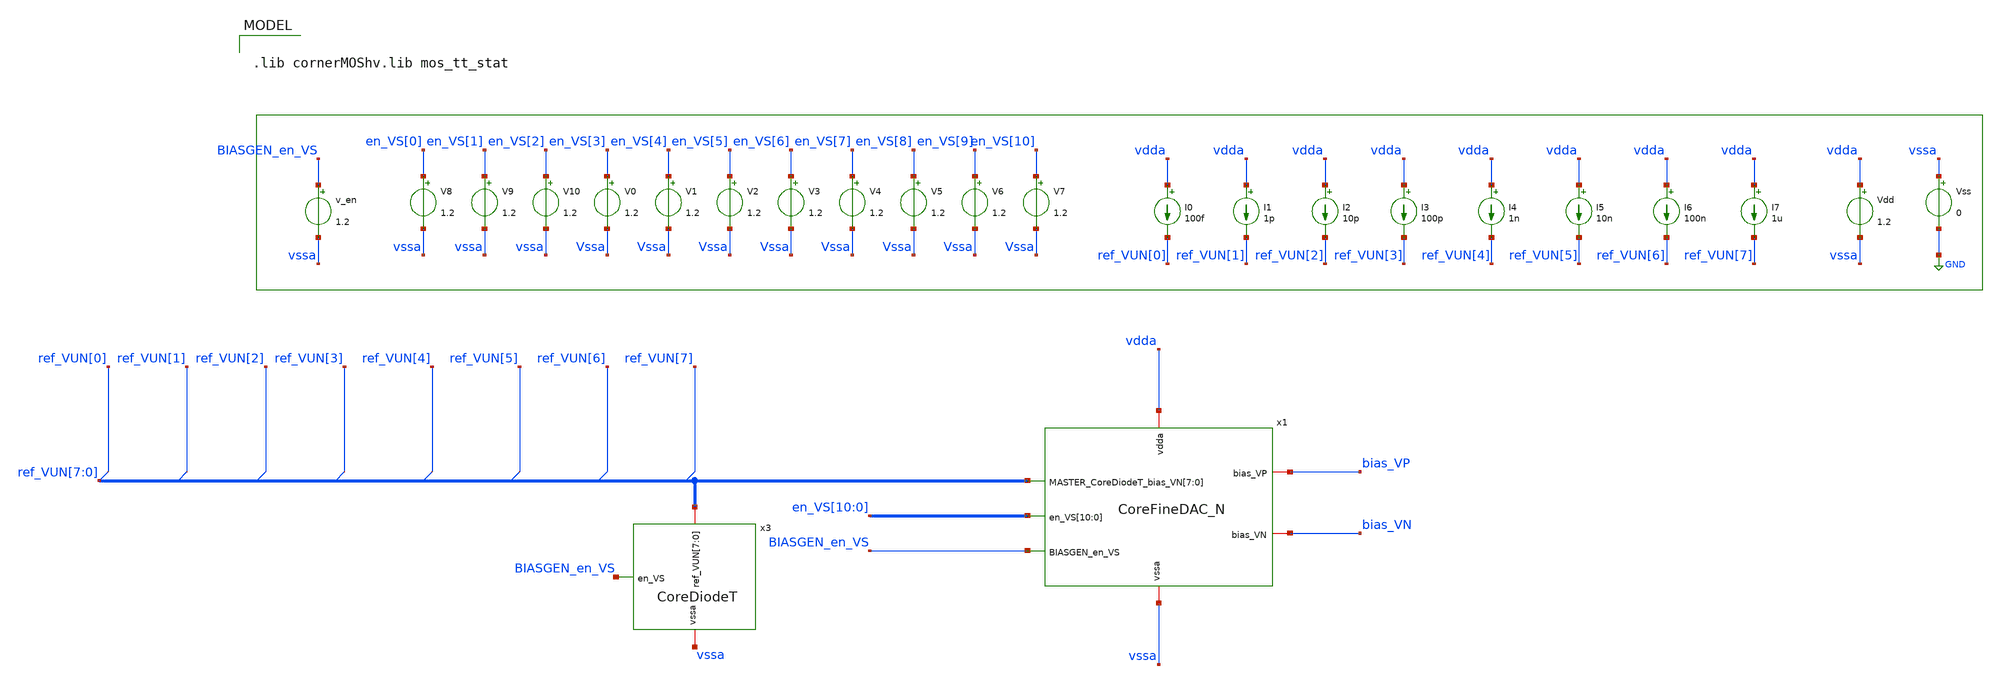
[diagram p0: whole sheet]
** sch_path: test_bench/CoreFineDAC_N_mc_dc_tb.sch
**.subckt CoreFineDAC_N_mc_dc_tb
Vdd vdda vssa 1.2
V0 en_VS[3] Vssa 1.2
Vss vssa GND 0
V1 en_VS[4] Vssa 1.2
V2 en_VS[5] Vssa 1.2
V3 en_VS[6] Vssa 1.2
V4 en_VS[7] Vssa 1.2
V5 en_VS[8] Vssa 1.2
V6 en_VS[9] Vssa 1.2
V7 en_VS[10] Vssa 1.2
V8 en_VS[0] vssa 1.2
V9 en_VS[1] vssa 1.2
V10 en_VS[2] vssa 1.2
I0 vdda ref_VUN[0] 100f
I1 vdda ref_VUN[1] 1p
I2 vdda ref_VUN[2] 10p
I3 vdda ref_VUN[3] 100p
I4 vdda ref_VUN[4] 1n
I6 vdda ref_VUN[6] 100n
I5 vdda ref_VUN[5] 10n
I7 vdda ref_VUN[7] 1u
v_en BIASGEN_en_VS vssa 1.2
x1 en_VS[10] en_VS[9] en_VS[8] en_VS[7] en_VS[6] en_VS[5] en_VS[4] en_VS[3] en_VS[2] en_VS[1]
+ en_VS[0] vssa vdda bias_VP bias_VN ref_VUN[7] ref_VUN[6] ref_VUN[5] ref_VUN[4] ref_VUN[3] ref_VUN[2]
+ ref_VUN[1] ref_VUN[0] BIASGEN_en_VS CoreFineDAC_N
x3 ref_VUN[7] ref_VUN[6] ref_VUN[5] ref_VUN[4] ref_VUN[3] ref_VUN[2] ref_VUN[1] ref_VUN[0] vssa
+ BIASGEN_en_VS CoreDiodeT
**** begin user architecture code

.lib cornerMOShv.lib mos_tt_stat



.param mm_ok=1
.param mc_ok=1
.param temp=27
.options abstol=1e-14
.options gmin=1e-14
.options gmindc=1e-14
.control


let mc_runs = 300
let run = 0
dowhile run < mc_runs

nodeset v(x2.VBIAS)=0.5 v(x2.x_ota.vout1stage)=0.7 v(x2.x_ota.vpmirr)=0.35
let V_drain_ISINK_vect = vector(1)
let initial_range = 7
let code_range = initial_range
let max_range = initial_range +1
let digitalCommand = vector(1)
let out_UP = vector(1)
let V_out_UP = vector(1)
let V_drain_ISINK_vect = vector(1)
let V_bias = vector(1)
while code_range < max_range
    * Set the 3 bits
    alter V8 = 1.2*(code_range % 2)
    alter V9 = 1.2*(floor(code_range/2) % 2)
    alter V10 = 1.2*(floor(code_range/4) % 2)
    let min = 0
    let max = 1
    let code = max-1
    while code < max
      save all
      * Set the 8 bits
      alter V0 = 1.2*(code % 2)
      alter V1 = 1.2*(floor(code/2) % 2)
      alter V2 = 1.2*(floor(code/4) % 2)
      alter V3 = 1.2*(floor(code/8) % 2)
      alter V4 = 1.2*(floor(code/16) % 2)
      alter V5 = 1.2*(floor(code/32) % 2)
      alter V6 = 1.2*(floor(code/64) % 2)
      alter V7 = 1.2*(floor(code/128) % 2)

      op

      let digitalCommand[0] = code
      let out_UP[0] = I(V.x1.V_out_UP)
      let V_out_UP[0] = V(bias_VP)
      let V_bias[0] = V(x1.bias_test)
      let V_drain_ISINK_vect[0] = V(x1.V_drain_ISINK)
      * let out_UP[code-min] = I(V.x1.V_Ibias)
      let code = code + 1
      * print code
      * write CoreFineDAC_N_dc_tb/full_op_{$&code_range}.raw


   end
   setplot const
   settype current out_UP
   settype voltage V_out_UP
   settype voltage V_drain_ISINK_vect
   settype voltage V_bias
   setscale digitalCommand
   * plot out_UP
   * plot V_out_UP
   * plot V_drain_ISINK_vect
   * plot V_bias

   let code_range = code_range + 1
   write  simulations/CoreFineDAC_N_mc_dc_tb/commandRange_{$&initial_range}_{$&max}_{$&run}.raw out_UP
   write CoreFineDAC_N_mc_dc_tb/commandRange_{$&initial_range}_{$&max}_{$&run}.raw out_UP
end

reset
let run=run+1
end


.endc





**** end user architecture code
**.ends
.GLOBAL GND
.end
